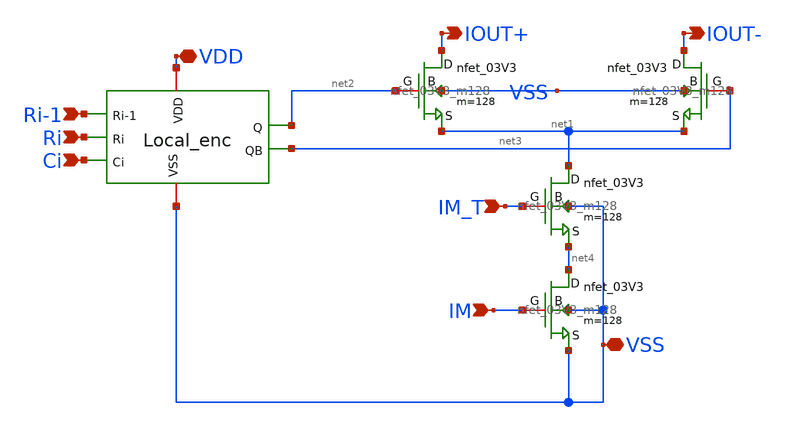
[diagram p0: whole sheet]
** sch_path: DAC_PAKISTAN_01/Pakistan1_Xschem/MSB_UNIT_CELL_V3.sch
**.subckt MSB_UNIT_CELL_V3 VDD VSS Ri-1 Ri Ci IM_T IM IOUT+ IOUT-
*.iopin VDD
*.iopin VSS
*.ipin Ri-1
*.ipin Ri
*.ipin Ci
*.ipin IM_T
*.ipin IM
*.opin IOUT+
*.opin IOUT-
x1 VDD VSS Ri-1 Ri Ci net2 net3 Local_Enc
x2 VSS net4 VSS IM nfet_03V3_m128
x3 net4 net1 VSS IM_T nfet_03V3_m128
x4 net1 IOUT+ VSS net2 nfet_03V3_m128
x5 net1 IOUT- VSS net3 nfet_03V3_m128
**.ends
.end
